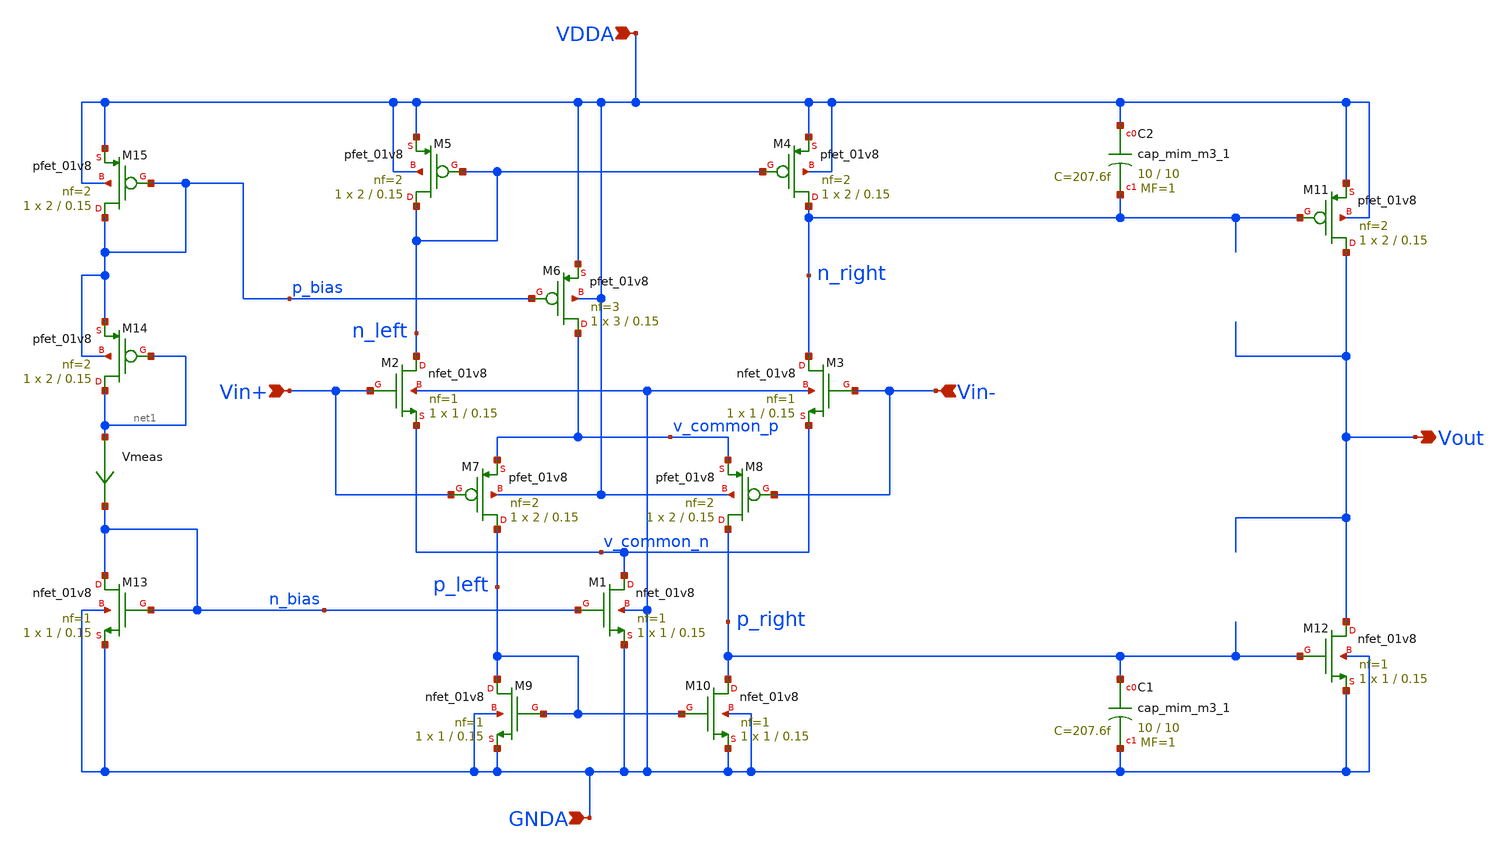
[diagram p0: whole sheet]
** sch_path: projects/pll/charge_pump/xschem_ngspice/rail_to_rail_opamp5.sch
**.subckt rail_to_rail_opamp5 Vout Vin+ Vin- VDDA GNDA
*.opin Vout
*.ipin Vin+
*.ipin Vin-
*.ipin VDDA
*.ipin GNDA
XM2 n_left Vin+ v_common_n GNDA sky130_fd_pr__nfet_01v8 L=0.15 W=1 nf=1 ad='int((nf+1)/2) * W/nf * 0.29'
+ as='int((nf+2)/2) * W/nf * 0.29' pd='2*int((nf+1)/2) * (W/nf + 0.29)' ps='2*int((nf+2)/2) * (W/nf + 0.29)'
+ nrd='0.29 / W' nrs='0.29 / W' sa=0 sb=0 sd=0 mult=1 m=1
XM3 n_right Vin- v_common_n GNDA sky130_fd_pr__nfet_01v8 L=0.15 W=1 nf=1 ad='int((nf+1)/2) * W/nf * 0.29'
+ as='int((nf+2)/2) * W/nf * 0.29' pd='2*int((nf+1)/2) * (W/nf + 0.29)' ps='2*int((nf+2)/2) * (W/nf + 0.29)'
+ nrd='0.29 / W' nrs='0.29 / W' sa=0 sb=0 sd=0 mult=1 m=1
XM5 n_left n_left VDDA VDDA sky130_fd_pr__pfet_01v8 L=0.15 W=2 nf=2 ad='int((nf+1)/2) * W/nf * 0.29'
+ as='int((nf+2)/2) * W/nf * 0.29' pd='2*int((nf+1)/2) * (W/nf + 0.29)' ps='2*int((nf+2)/2) * (W/nf + 0.29)'
+ nrd='0.29 / W' nrs='0.29 / W' sa=0 sb=0 sd=0 mult=1 m=1
XM4 n_right n_left VDDA VDDA sky130_fd_pr__pfet_01v8 L=0.15 W=2 nf=2 ad='int((nf+1)/2) * W/nf * 0.29'
+ as='int((nf+2)/2) * W/nf * 0.29' pd='2*int((nf+1)/2) * (W/nf + 0.29)' ps='2*int((nf+2)/2) * (W/nf + 0.29)'
+ nrd='0.29 / W' nrs='0.29 / W' sa=0 sb=0 sd=0 mult=1 m=1
XM6 v_common_p p_bias VDDA VDDA sky130_fd_pr__pfet_01v8 L=0.15 W=3 nf=3 ad='int((nf+1)/2) * W/nf * 0.29'
+ as='int((nf+2)/2) * W/nf * 0.29' pd='2*int((nf+1)/2) * (W/nf + 0.29)' ps='2*int((nf+2)/2) * (W/nf + 0.29)'
+ nrd='0.29 / W' nrs='0.29 / W' sa=0 sb=0 sd=0 mult=1 m=1
XM7 p_left Vin+ v_common_p VDDA sky130_fd_pr__pfet_01v8 L=0.15 W=2 nf=2 ad='int((nf+1)/2) * W/nf * 0.29'
+ as='int((nf+2)/2) * W/nf * 0.29' pd='2*int((nf+1)/2) * (W/nf + 0.29)' ps='2*int((nf+2)/2) * (W/nf + 0.29)'
+ nrd='0.29 / W' nrs='0.29 / W' sa=0 sb=0 sd=0 mult=1 m=1
XM8 p_right Vin- v_common_p VDDA sky130_fd_pr__pfet_01v8 L=0.15 W=2 nf=2 ad='int((nf+1)/2) * W/nf * 0.29'
+ as='int((nf+2)/2) * W/nf * 0.29' pd='2*int((nf+1)/2) * (W/nf + 0.29)' ps='2*int((nf+2)/2) * (W/nf + 0.29)'
+ nrd='0.29 / W' nrs='0.29 / W' sa=0 sb=0 sd=0 mult=1 m=1
XM9 p_left p_left GNDA GNDA sky130_fd_pr__nfet_01v8 L=0.15 W=1 nf=1 ad='int((nf+1)/2) * W/nf * 0.29'
+ as='int((nf+2)/2) * W/nf * 0.29' pd='2*int((nf+1)/2) * (W/nf + 0.29)' ps='2*int((nf+2)/2) * (W/nf + 0.29)'
+ nrd='0.29 / W' nrs='0.29 / W' sa=0 sb=0 sd=0 mult=1 m=1
XM10 p_right p_left GNDA GNDA sky130_fd_pr__nfet_01v8 L=0.15 W=1 nf=1 ad='int((nf+1)/2) * W/nf * 0.29'
+ as='int((nf+2)/2) * W/nf * 0.29' pd='2*int((nf+1)/2) * (W/nf + 0.29)' ps='2*int((nf+2)/2) * (W/nf + 0.29)'
+ nrd='0.29 / W' nrs='0.29 / W' sa=0 sb=0 sd=0 mult=1 m=1
XM1 v_common_n n_bias GNDA GNDA sky130_fd_pr__nfet_01v8 L=0.15 W=1 nf=1 ad='int((nf+1)/2) * W/nf * 0.29'
+ as='int((nf+2)/2) * W/nf * 0.29' pd='2*int((nf+1)/2) * (W/nf + 0.29)' ps='2*int((nf+2)/2) * (W/nf + 0.29)'
+ nrd='0.29 / W' nrs='0.29 / W' sa=0 sb=0 sd=0 mult=1 m=1
XM11 Vout n_right VDDA VDDA sky130_fd_pr__pfet_01v8 L=0.15 W=2 nf=2 ad='int((nf+1)/2) * W/nf * 0.29'
+ as='int((nf+2)/2) * W/nf * 0.29' pd='2*int((nf+1)/2) * (W/nf + 0.29)' ps='2*int((nf+2)/2) * (W/nf + 0.29)'
+ nrd='0.29 / W' nrs='0.29 / W' sa=0 sb=0 sd=0 mult=1 m=1
XM12 Vout p_right GNDA GNDA sky130_fd_pr__nfet_01v8 L=0.15 W=1 nf=1 ad='int((nf+1)/2) * W/nf * 0.29'
+ as='int((nf+2)/2) * W/nf * 0.29' pd='2*int((nf+1)/2) * (W/nf + 0.29)' ps='2*int((nf+2)/2) * (W/nf + 0.29)'
+ nrd='0.29 / W' nrs='0.29 / W' sa=0 sb=0 sd=0 mult=1 m=1
XM13 n_bias n_bias GNDA GNDA sky130_fd_pr__nfet_01v8 L=0.15 W=1 nf=1 ad='int((nf+1)/2) * W/nf * 0.29'
+ as='int((nf+2)/2) * W/nf * 0.29' pd='2*int((nf+1)/2) * (W/nf + 0.29)' ps='2*int((nf+2)/2) * (W/nf + 0.29)'
+ nrd='0.29 / W' nrs='0.29 / W' sa=0 sb=0 sd=0 mult=1 m=1
XM15 p_bias p_bias VDDA VDDA sky130_fd_pr__pfet_01v8 L=0.15 W=2 nf=2 ad='int((nf+1)/2) * W/nf * 0.29'
+ as='int((nf+2)/2) * W/nf * 0.29' pd='2*int((nf+1)/2) * (W/nf + 0.29)' ps='2*int((nf+2)/2) * (W/nf + 0.29)'
+ nrd='0.29 / W' nrs='0.29 / W' sa=0 sb=0 sd=0 mult=1 m=1
Vmeas net1 n_bias 0
.save i(vmeas)
XM14 net1 net1 p_bias p_bias sky130_fd_pr__pfet_01v8 L=0.15 W=2 nf=2 ad='int((nf+1)/2) * W/nf * 0.29'
+ as='int((nf+2)/2) * W/nf * 0.29' pd='2*int((nf+1)/2) * (W/nf + 0.29)' ps='2*int((nf+2)/2) * (W/nf + 0.29)'
+ nrd='0.29 / W' nrs='0.29 / W' sa=0 sb=0 sd=0 mult=1 m=1
XC1 p_right GNDA sky130_fd_pr__cap_mim_m3_1 W=10 L=10 MF=1 m=1
XC2 VDDA n_right sky130_fd_pr__cap_mim_m3_1 W=10 L=10 MF=1 m=1
**.ends
.end
